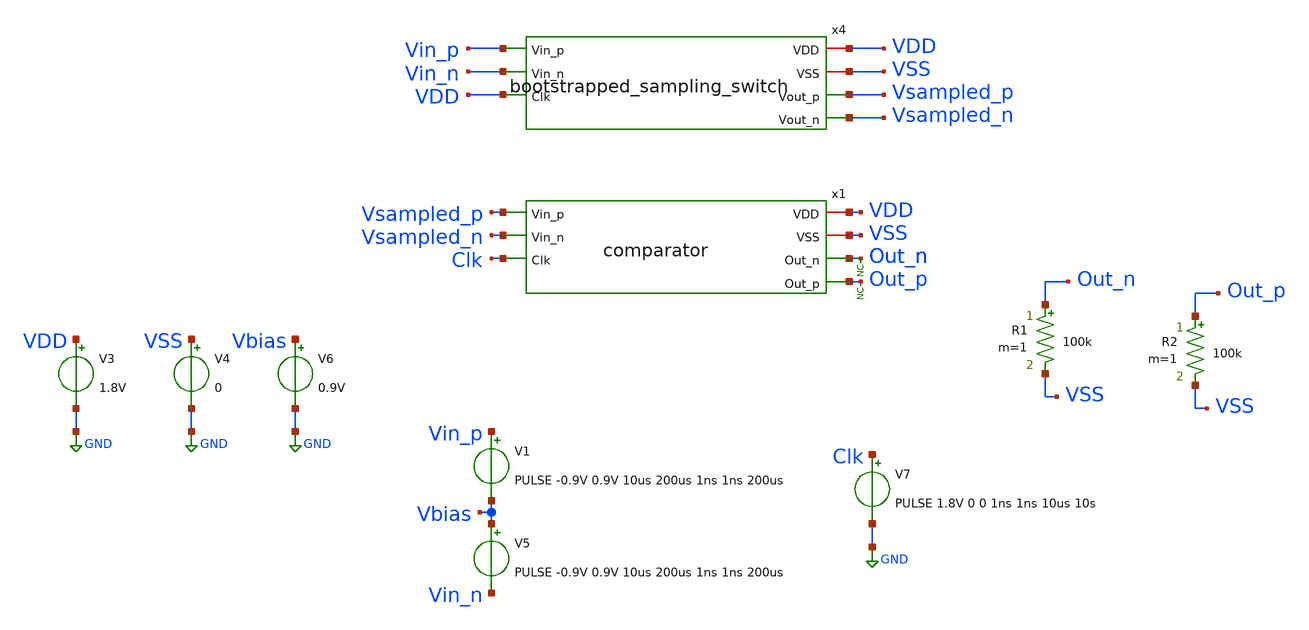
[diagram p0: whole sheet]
** sch_path: xschem/tests/comparator/comparator_sw_test.sch
**.subckt comparator_sw_test
V3 VDD GND 1.8V
V4 VSS GND 0
x1 VDD VSS Vsampled_p Out_n Vsampled_n Out_p Clk comparator
* noconn Out_p
* noconn Out_n
V6 Vbias GND 0.9V
R1 Out_n VSS 100k m=1
R2 Out_p VSS 100k m=1
x4 VDD Vin_p VSS Vin_n VDD Vsampled_p Vsampled_n bootstrapped_sampling_switch
V7 Clk GND PULSE 1.8V 0 0 1ns 1ns 10us 10s
V1 Vin_p Vbias PULSE -0.9V 0.9V 10us 200us 1ns 1ns 200us
V5 Vbias Vin_n PULSE -0.9V 0.9V 10us 200us 1ns 1ns 200us
**** begin user architecture code
 .lib $::SKYWATER_MODELS/sky130.lib.spice tt
.include $::SKYWATER_STDCELLS/sky130_fd_sc_hd.spice


.options acct list
.temp 25
*vvcc VDD 0 dc 1.8
*vvss VSS 0 0

.control
tran 0.05u 200u
*dc V1 0 1.8V 0.1
plot Vin_p-Vin_n Out_p-Out_n Clk-4
plot Vin_p-Vin_n x1.pre_amp_p-x1.pre_amp_n Clk-4
plot vsampled_p vsampled_n
write comparator_sw_test.raw
.endc


**** end user architecture code
**.ends

* expanding   symbol:  src/comparator/comparator.sym # of pins=7
** sym_path: xschem/src/comparator/comparator.sym
** sch_path: xschem/src/comparator/comparator.sch
.subckt comparator VDD VSS Vin_p Out_n Vin_n Out_p Clk
*.iopin VDD
*.iopin VSS
*.ipin Vin_p
*.opin Out_n
*.ipin Vin_n
*.opin Out_p
*.ipin Clk
XM1 Pre_Amp_n Clk VDD VSS sky130_fd_pr__pfet_01v8 L=0.15 W=1 nf=1 ad='int((nf+1)/2) * W/nf * 0.29' as='int((nf+2)/2) * W/nf * 0.29'
+ pd='2*int((nf+1)/2) * (W/nf + 0.29)' ps='2*int((nf+2)/2) * (W/nf + 0.29)' nrd='0.29 / W' nrs='0.29 / W'
+ sa=0 sb=0 sd=0 mult=1 m=1
XM2 Pre_Amp_p Clk VDD VSS sky130_fd_pr__pfet_01v8 L=0.15 W=1 nf=1 ad='int((nf+1)/2) * W/nf * 0.29' as='int((nf+2)/2) * W/nf * 0.29'
+ pd='2*int((nf+1)/2) * (W/nf + 0.29)' ps='2*int((nf+2)/2) * (W/nf + 0.29)' nrd='0.29 / W' nrs='0.29 / W'
+ sa=0 sb=0 sd=0 mult=1 m=1
XM3 Pre_Amp_p Vin_p net1 VSS sky130_fd_pr__nfet_01v8 L=0.15 W=1 nf=1 ad='int((nf+1)/2) * W/nf * 0.29'
+ as='int((nf+2)/2) * W/nf * 0.29' pd='2*int((nf+1)/2) * (W/nf + 0.29)' ps='2*int((nf+2)/2) * (W/nf + 0.29)'
+ nrd='0.29 / W' nrs='0.29 / W' sa=0 sb=0 sd=0 mult=1 m=1
XM4 Pre_Amp_n Vin_n net1 VSS sky130_fd_pr__nfet_01v8 L=0.15 W=1 nf=1 ad='int((nf+1)/2) * W/nf * 0.29'
+ as='int((nf+2)/2) * W/nf * 0.29' pd='2*int((nf+1)/2) * (W/nf + 0.29)' ps='2*int((nf+2)/2) * (W/nf + 0.29)'
+ nrd='0.29 / W' nrs='0.29 / W' sa=0 sb=0 sd=0 mult=1 m=1
XM5 net3 Out_p VDD VSS sky130_fd_pr__pfet_01v8 L=0.15 W=1 nf=1 ad='int((nf+1)/2) * W/nf * 0.29' as='int((nf+2)/2) * W/nf * 0.29'
+ pd='2*int((nf+1)/2) * (W/nf + 0.29)' ps='2*int((nf+2)/2) * (W/nf + 0.29)' nrd='0.29 / W' nrs='0.29 / W'
+ sa=0 sb=0 sd=0 mult=1 m=1
XM6 net2 Out_n VDD VSS sky130_fd_pr__pfet_01v8 L=0.15 W=1 nf=1 ad='int((nf+1)/2) * W/nf * 0.29' as='int((nf+2)/2) * W/nf * 0.29'
+ pd='2*int((nf+1)/2) * (W/nf + 0.29)' ps='2*int((nf+2)/2) * (W/nf + 0.29)' nrd='0.29 / W' nrs='0.29 / W'
+ sa=0 sb=0 sd=0 mult=1 m=1
XM7 net2 Pre_Amp_p Out_p VSS sky130_fd_pr__nfet_01v8 L=0.15 W=1 nf=1 ad='int((nf+1)/2) * W/nf * 0.29'
+ as='int((nf+2)/2) * W/nf * 0.29' pd='2*int((nf+1)/2) * (W/nf + 0.29)' ps='2*int((nf+2)/2) * (W/nf + 0.29)'
+ nrd='0.29 / W' nrs='0.29 / W' sa=0 sb=0 sd=0 mult=1 m=1
XM8 net3 Pre_Amp_n Out_n VSS sky130_fd_pr__nfet_01v8 L=0.15 W=1 nf=1 ad='int((nf+1)/2) * W/nf * 0.29'
+ as='int((nf+2)/2) * W/nf * 0.29' pd='2*int((nf+1)/2) * (W/nf + 0.29)' ps='2*int((nf+2)/2) * (W/nf + 0.29)'
+ nrd='0.29 / W' nrs='0.29 / W' sa=0 sb=0 sd=0 mult=1 m=1
XM9 net1 Clk VSS VSS sky130_fd_pr__nfet_01v8 L=0.15 W=1 nf=1 ad='int((nf+1)/2) * W/nf * 0.29' as='int((nf+2)/2) * W/nf * 0.29'
+ pd='2*int((nf+1)/2) * (W/nf + 0.29)' ps='2*int((nf+2)/2) * (W/nf + 0.29)' nrd='0.29 / W' nrs='0.29 / W'
+ sa=0 sb=0 sd=0 mult=1 m=1
XM10 Pre_Amp_n Vin_n net1 VSS sky130_fd_pr__nfet_01v8 L=0.15 W=1 nf=1 ad='int((nf+1)/2) * W/nf * 0.29'
+ as='int((nf+2)/2) * W/nf * 0.29' pd='2*int((nf+1)/2) * (W/nf + 0.29)' ps='2*int((nf+2)/2) * (W/nf + 0.29)'
+ nrd='0.29 / W' nrs='0.29 / W' sa=0 sb=0 sd=0 mult=1 m=1
XM11 Out_n Clk_n VSS VSS sky130_fd_pr__nfet_01v8 L=0.15 W=1 nf=1 ad='int((nf+1)/2) * W/nf * 0.29' as='int((nf+2)/2) * W/nf * 0.29'
+ pd='2*int((nf+1)/2) * (W/nf + 0.29)' ps='2*int((nf+2)/2) * (W/nf + 0.29)' nrd='0.29 / W' nrs='0.29 / W'
+ sa=0 sb=0 sd=0 mult=1 m=1
XM12 Out_n Out_p VSS VSS sky130_fd_pr__nfet_01v8 L=0.15 W=1 nf=1 ad='int((nf+1)/2) * W/nf * 0.29' as='int((nf+2)/2) * W/nf * 0.29'
+ pd='2*int((nf+1)/2) * (W/nf + 0.29)' ps='2*int((nf+2)/2) * (W/nf + 0.29)' nrd='0.29 / W' nrs='0.29 / W'
+ sa=0 sb=0 sd=0 mult=1 m=1
XM13 Out_p Out_n VSS VSS sky130_fd_pr__nfet_01v8 L=0.15 W=1 nf=1 ad='int((nf+1)/2) * W/nf * 0.29' as='int((nf+2)/2) * W/nf * 0.29'
+ pd='2*int((nf+1)/2) * (W/nf + 0.29)' ps='2*int((nf+2)/2) * (W/nf + 0.29)' nrd='0.29 / W' nrs='0.29 / W'
+ sa=0 sb=0 sd=0 mult=1 m=1
XM14 Out_p Clk_n VSS VSS sky130_fd_pr__nfet_01v8 L=0.15 W=1 nf=1 ad='int((nf+1)/2) * W/nf * 0.29' as='int((nf+2)/2) * W/nf * 0.29'
+ pd='2*int((nf+1)/2) * (W/nf + 0.29)' ps='2*int((nf+2)/2) * (W/nf + 0.29)' nrd='0.29 / W' nrs='0.29 / W'
+ sa=0 sb=0 sd=0 mult=1 m=1
XM15 Clk_n Clk VDD VSS sky130_fd_pr__pfet_01v8 L=0.15 W=1 nf=1 ad='int((nf+1)/2) * W/nf * 0.29' as='int((nf+2)/2) * W/nf * 0.29'
+ pd='2*int((nf+1)/2) * (W/nf + 0.29)' ps='2*int((nf+2)/2) * (W/nf + 0.29)' nrd='0.29 / W' nrs='0.29 / W'
+ sa=0 sb=0 sd=0 mult=1 m=1
XM16 Clk_n Clk VSS VSS sky130_fd_pr__nfet_01v8 L=0.15 W=1 nf=1 ad='int((nf+1)/2) * W/nf * 0.29' as='int((nf+2)/2) * W/nf * 0.29'
+ pd='2*int((nf+1)/2) * (W/nf + 0.29)' ps='2*int((nf+2)/2) * (W/nf + 0.29)' nrd='0.29 / W' nrs='0.29 / W'
+ sa=0 sb=0 sd=0 mult=1 m=1
.ends


* expanding   symbol:  src/bootstrapped_sampling_switch/bootstrapped_sampling_switch.sym # of pins=7
** sym_path: xschem/src/bootstrapped_sampling_switch/bootstrapped_sampling_switch.sym
** sch_path: xschem/src/bootstrapped_sampling_switch/bootstrapped_sampling_switch.sch
.subckt bootstrapped_sampling_switch VDD Vin_p VSS Vin_n Clk Vout_p Vout_n
*.iopin VDD
*.ipin Vin_p
*.opin Vout_p
*.iopin VSS
*.opin Vout_n
*.ipin Vin_n
*.ipin Clk
XM1 net3 Clk_n VSS VSS sky130_fd_pr__nfet_01v8 L=0.15 W=0.91 nf=1 ad='int((nf+1)/2) * W/nf * 0.29' as='int((nf+2)/2) * W/nf * 0.29'
+ pd='2*int((nf+1)/2) * (W/nf + 0.29)' ps='2*int((nf+2)/2) * (W/nf + 0.29)' nrd='0.29 / W' nrs='0.29 / W'
+ sa=0 sb=0 sd=0 mult=8 m=8
XM2 net1 Clk VDD VDD sky130_fd_pr__pfet_01v8 L=0.15 W=1.605 nf=1 ad='int((nf+1)/2) * W/nf * 0.29' as='int((nf+2)/2) * W/nf * 0.29'
+ pd='2*int((nf+1)/2) * (W/nf + 0.29)' ps='2*int((nf+2)/2) * (W/nf + 0.29)' nrd='0.29 / W' nrs='0.29 / W'
+ sa=0 sb=0 sd=0 mult=1 m=1
XM3 net1 Clk net3 VSS sky130_fd_pr__nfet_01v8 L=0.15 W=0.91 nf=1 ad='int((nf+1)/2) * W/nf * 0.29' as='int((nf+2)/2) * W/nf * 0.29'
+ pd='2*int((nf+1)/2) * (W/nf + 0.29)' ps='2*int((nf+2)/2) * (W/nf + 0.29)' nrd='0.29 / W' nrs='0.29 / W'
+ sa=0 sb=0 sd=0 mult=1 m=1
XC1 net2 net3 sky130_fd_pr__cap_mim_m3_1 W=50 L=50 MF=1 m=1
XM4 net2 net4 VDD net2 sky130_fd_pr__pfet_01v8 L=0.15 W=0.91 nf=1 ad='int((nf+1)/2) * W/nf * 0.29' as='int((nf+2)/2) * W/nf * 0.29'
+ pd='2*int((nf+1)/2) * (W/nf + 0.29)' ps='2*int((nf+2)/2) * (W/nf + 0.29)' nrd='0.29 / W' nrs='0.29 / W'
+ sa=0 sb=0 sd=0 mult=1 m=1
XM5 net4 net1 net2 net2 sky130_fd_pr__pfet_01v8 L=0.15 W=1.605 nf=1 ad='int((nf+1)/2) * W/nf * 0.29'
+ as='int((nf+2)/2) * W/nf * 0.29' pd='2*int((nf+1)/2) * (W/nf + 0.29)' ps='2*int((nf+2)/2) * (W/nf + 0.29)'
+ nrd='0.29 / W' nrs='0.29 / W' sa=0 sb=0 sd=0 mult=1 m=1
XM6 net1 net4 net3 VSS sky130_fd_pr__nfet_01v8 L=0.15 W=0.91 nf=1 ad='int((nf+1)/2) * W/nf * 0.29' as='int((nf+2)/2) * W/nf * 0.29'
+ pd='2*int((nf+1)/2) * (W/nf + 0.29)' ps='2*int((nf+2)/2) * (W/nf + 0.29)' nrd='0.29 / W' nrs='0.29 / W'
+ sa=0 sb=0 sd=0 mult=1 m=1
XM7 Vin_p net4 net3 VSS sky130_fd_pr__nfet_01v8 L=0.15 W=0.91 nf=1 ad='int((nf+1)/2) * W/nf * 0.29' as='int((nf+2)/2) * W/nf * 0.29'
+ pd='2*int((nf+1)/2) * (W/nf + 0.29)' ps='2*int((nf+2)/2) * (W/nf + 0.29)' nrd='0.29 / W' nrs='0.29 / W'
+ sa=0 sb=0 sd=0 mult=1 m=1
XM8 Vin_p net4 Vout_p VSS sky130_fd_pr__nfet_01v8 L=0.15 W=0.91 nf=1 ad='int((nf+1)/2) * W/nf * 0.29'
+ as='int((nf+2)/2) * W/nf * 0.29' pd='2*int((nf+1)/2) * (W/nf + 0.29)' ps='2*int((nf+2)/2) * (W/nf + 0.29)'
+ nrd='0.29 / W' nrs='0.29 / W' sa=0 sb=0 sd=0 mult=75 m=75
XM9 net4 VDD net5 VSS sky130_fd_pr__nfet_01v8 L=0.15 W=0.91 nf=1 ad='int((nf+1)/2) * W/nf * 0.29' as='int((nf+2)/2) * W/nf * 0.29'
+ pd='2*int((nf+1)/2) * (W/nf + 0.29)' ps='2*int((nf+2)/2) * (W/nf + 0.29)' nrd='0.29 / W' nrs='0.29 / W'
+ sa=0 sb=0 sd=0 mult=2 m=2
XM10 net5 Clk_n VSS VSS sky130_fd_pr__nfet_01v8 L=0.15 W=0.91 nf=1 ad='int((nf+1)/2) * W/nf * 0.29' as='int((nf+2)/2) * W/nf * 0.29'
+ pd='2*int((nf+1)/2) * (W/nf + 0.29)' ps='2*int((nf+2)/2) * (W/nf + 0.29)' nrd='0.29 / W' nrs='0.29 / W'
+ sa=0 sb=0 sd=0 mult=1 m=1
x1 Clk VSS VSS VDD VDD Clk_n sky130_fd_sc_hd__clkinv_1
XM11 net8 Clk_n VSS VSS sky130_fd_pr__nfet_01v8 L=0.15 W=0.91 nf=1 ad='int((nf+1)/2) * W/nf * 0.29' as='int((nf+2)/2) * W/nf * 0.29'
+ pd='2*int((nf+1)/2) * (W/nf + 0.29)' ps='2*int((nf+2)/2) * (W/nf + 0.29)' nrd='0.29 / W' nrs='0.29 / W'
+ sa=0 sb=0 sd=0 mult=8 m=8
XM12 net6 Clk VDD VDD sky130_fd_pr__pfet_01v8 L=0.15 W=1.605 nf=1 ad='int((nf+1)/2) * W/nf * 0.29' as='int((nf+2)/2) * W/nf * 0.29'
+ pd='2*int((nf+1)/2) * (W/nf + 0.29)' ps='2*int((nf+2)/2) * (W/nf + 0.29)' nrd='0.29 / W' nrs='0.29 / W'
+ sa=0 sb=0 sd=0 mult=1 m=1
XM13 net6 Clk net8 VSS sky130_fd_pr__nfet_01v8 L=0.15 W=0.91 nf=1 ad='int((nf+1)/2) * W/nf * 0.29' as='int((nf+2)/2) * W/nf * 0.29'
+ pd='2*int((nf+1)/2) * (W/nf + 0.29)' ps='2*int((nf+2)/2) * (W/nf + 0.29)' nrd='0.29 / W' nrs='0.29 / W'
+ sa=0 sb=0 sd=0 mult=1 m=1
XC2 net7 net8 sky130_fd_pr__cap_mim_m3_1 W=50 L=50 MF=1 m=1
XM14 net7 net9 VDD net7 sky130_fd_pr__pfet_01v8 L=0.15 W=0.91 nf=1 ad='int((nf+1)/2) * W/nf * 0.29' as='int((nf+2)/2) * W/nf * 0.29'
+ pd='2*int((nf+1)/2) * (W/nf + 0.29)' ps='2*int((nf+2)/2) * (W/nf + 0.29)' nrd='0.29 / W' nrs='0.29 / W'
+ sa=0 sb=0 sd=0 mult=1 m=1
XM15 net9 net6 net7 net7 sky130_fd_pr__pfet_01v8 L=0.15 W=1.605 nf=1 ad='int((nf+1)/2) * W/nf * 0.29'
+ as='int((nf+2)/2) * W/nf * 0.29' pd='2*int((nf+1)/2) * (W/nf + 0.29)' ps='2*int((nf+2)/2) * (W/nf + 0.29)'
+ nrd='0.29 / W' nrs='0.29 / W' sa=0 sb=0 sd=0 mult=1 m=1
XM16 net6 net9 net8 VSS sky130_fd_pr__nfet_01v8 L=0.15 W=0.91 nf=1 ad='int((nf+1)/2) * W/nf * 0.29' as='int((nf+2)/2) * W/nf * 0.29'
+ pd='2*int((nf+1)/2) * (W/nf + 0.29)' ps='2*int((nf+2)/2) * (W/nf + 0.29)' nrd='0.29 / W' nrs='0.29 / W'
+ sa=0 sb=0 sd=0 mult=1 m=1
XM17 Vin_n net9 net8 VSS sky130_fd_pr__nfet_01v8 L=0.15 W=0.91 nf=1 ad='int((nf+1)/2) * W/nf * 0.29'
+ as='int((nf+2)/2) * W/nf * 0.29' pd='2*int((nf+1)/2) * (W/nf + 0.29)' ps='2*int((nf+2)/2) * (W/nf + 0.29)'
+ nrd='0.29 / W' nrs='0.29 / W' sa=0 sb=0 sd=0 mult=1 m=1
XM18 Vin_n net9 Vout_n VSS sky130_fd_pr__nfet_01v8 L=0.15 W=0.91 nf=1 ad='int((nf+1)/2) * W/nf * 0.29'
+ as='int((nf+2)/2) * W/nf * 0.29' pd='2*int((nf+1)/2) * (W/nf + 0.29)' ps='2*int((nf+2)/2) * (W/nf + 0.29)'
+ nrd='0.29 / W' nrs='0.29 / W' sa=0 sb=0 sd=0 mult=75 m=75
XM19 net9 VDD net10 VSS sky130_fd_pr__nfet_01v8 L=0.15 W=0.91 nf=1 ad='int((nf+1)/2) * W/nf * 0.29' as='int((nf+2)/2) * W/nf * 0.29'
+ pd='2*int((nf+1)/2) * (W/nf + 0.29)' ps='2*int((nf+2)/2) * (W/nf + 0.29)' nrd='0.29 / W' nrs='0.29 / W'
+ sa=0 sb=0 sd=0 mult=2 m=2
XM20 net10 Clk_n VSS VSS sky130_fd_pr__nfet_01v8 L=0.15 W=0.91 nf=1 ad='int((nf+1)/2) * W/nf * 0.29'
+ as='int((nf+2)/2) * W/nf * 0.29' pd='2*int((nf+1)/2) * (W/nf + 0.29)' ps='2*int((nf+2)/2) * (W/nf + 0.29)'
+ nrd='0.29 / W' nrs='0.29 / W' sa=0 sb=0 sd=0 mult=1 m=1
.ends

.GLOBAL GND
.end
